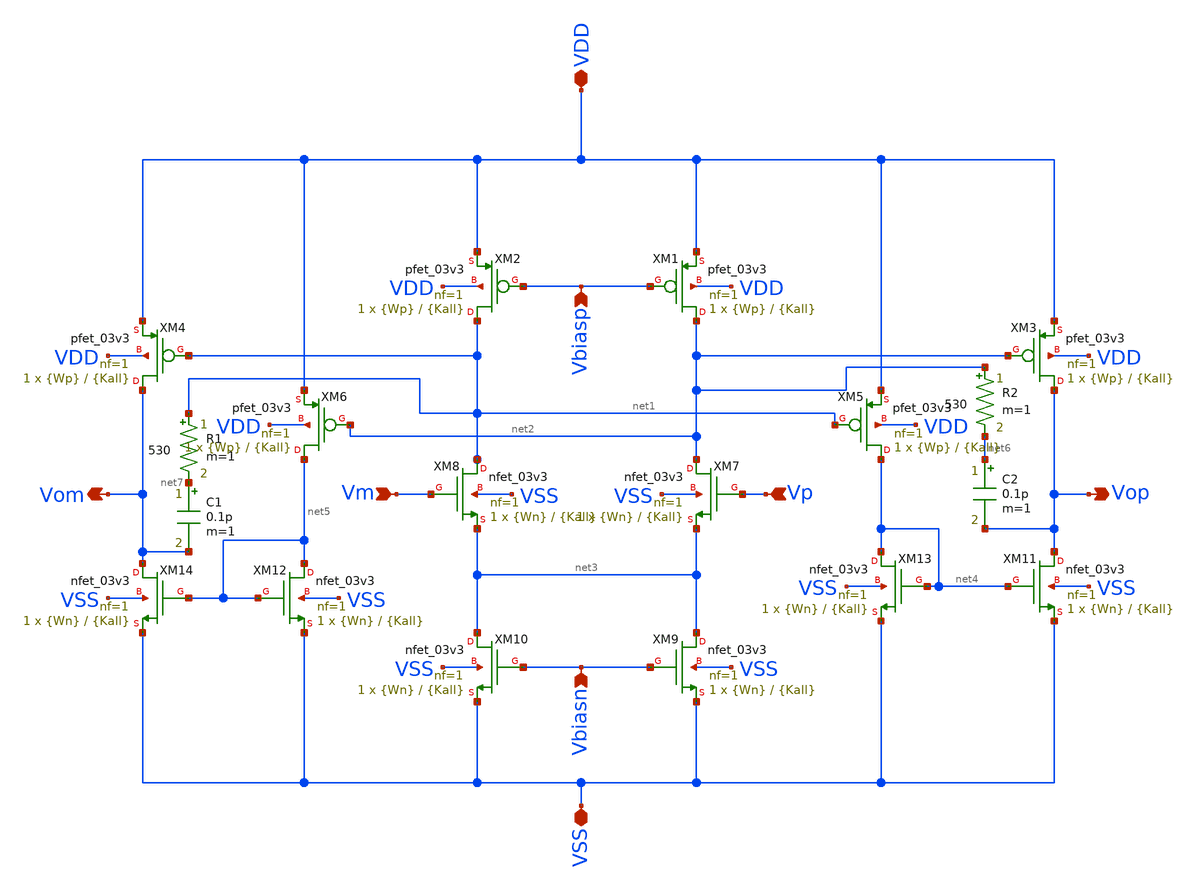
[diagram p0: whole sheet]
** sch_path: src/schematics/fully_differential_amplifier/fullydiffamp.sch
**.subckt fullydiffamp VDD VSS Vbiasn Vbiasp Vm Vp Vom Vop
*.iopin VDD
*.iopin VSS
*.ipin Vbiasn
*.ipin Vbiasp
*.ipin Vm
*.ipin Vp
*.opin Vom
*.opin Vop
XM5 net4 net1 VDD VDD pfet_03v3 L={Kall} W={Wp} nf=1 ad='int((nf+1)/2) * W/nf * 0.18u' as='int((nf+2)/2) * W/nf * 0.18u'
+ pd='2*int((nf+1)/2) * (W/nf + 0.18u)' ps='2*int((nf+2)/2) * (W/nf + 0.18u)' nrd='0.18u / W' nrs='0.18u / W'
+ sa=0 sb=0 sd=0 m=1
XM2 net1 Vbiasp VDD VDD pfet_03v3 L={Kall} W={Wp} nf=1 ad='int((nf+1)/2) * W/nf * 0.18u' as='int((nf+2)/2) * W/nf * 0.18u'
+ pd='2*int((nf+1)/2) * (W/nf + 0.18u)' ps='2*int((nf+2)/2) * (W/nf + 0.18u)' nrd='0.18u / W' nrs='0.18u / W'
+ sa=0 sb=0 sd=0 m=1
XM8 net1 Vm net3 VSS nfet_03v3 L={Kall} W={Wn} nf=1 ad='int((nf+1)/2) * W/nf * 0.18u' as='int((nf+2)/2) * W/nf * 0.18u'
+ pd='2*int((nf+1)/2) * (W/nf + 0.18u)' ps='2*int((nf+2)/2) * (W/nf + 0.18u)' nrd='0.18u / W' nrs='0.18u / W'
+ sa=0 sb=0 sd=0 m=1
XM7 net2 Vp net3 VSS nfet_03v3 L={Kall} W={Wn} nf=1 ad='int((nf+1)/2) * W/nf * 0.18u' as='int((nf+2)/2) * W/nf * 0.18u'
+ pd='2*int((nf+1)/2) * (W/nf + 0.18u)' ps='2*int((nf+2)/2) * (W/nf + 0.18u)' nrd='0.18u / W' nrs='0.18u / W'
+ sa=0 sb=0 sd=0 m=1
XM1 net2 Vbiasp VDD VDD pfet_03v3 L={Kall} W={Wp} nf=1 ad='int((nf+1)/2) * W/nf * 0.18u' as='int((nf+2)/2) * W/nf * 0.18u'
+ pd='2*int((nf+1)/2) * (W/nf + 0.18u)' ps='2*int((nf+2)/2) * (W/nf + 0.18u)' nrd='0.18u / W' nrs='0.18u / W'
+ sa=0 sb=0 sd=0 m=1
XM6 net5 net2 VDD VDD pfet_03v3 L={Kall} W={Wp} nf=1 ad='int((nf+1)/2) * W/nf * 0.18u' as='int((nf+2)/2) * W/nf * 0.18u'
+ pd='2*int((nf+1)/2) * (W/nf + 0.18u)' ps='2*int((nf+2)/2) * (W/nf + 0.18u)' nrd='0.18u / W' nrs='0.18u / W'
+ sa=0 sb=0 sd=0 m=1
XM4 Vom net1 VDD VDD pfet_03v3 L={Kall} W={Wp} nf=1 ad='int((nf+1)/2) * W/nf * 0.18u' as='int((nf+2)/2) * W/nf * 0.18u'
+ pd='2*int((nf+1)/2) * (W/nf + 0.18u)' ps='2*int((nf+2)/2) * (W/nf + 0.18u)' nrd='0.18u / W' nrs='0.18u / W'
+ sa=0 sb=0 sd=0 m=1
XM3 Vop net2 VDD VDD pfet_03v3 L={Kall} W={Wp} nf=1 ad='int((nf+1)/2) * W/nf * 0.18u' as='int((nf+2)/2) * W/nf * 0.18u'
+ pd='2*int((nf+1)/2) * (W/nf + 0.18u)' ps='2*int((nf+2)/2) * (W/nf + 0.18u)' nrd='0.18u / W' nrs='0.18u / W'
+ sa=0 sb=0 sd=0 m=1
XM9 net3 Vbiasn VSS VSS nfet_03v3 L={Kall} W={Wn} nf=1 ad='int((nf+1)/2) * W/nf * 0.18u' as='int((nf+2)/2) * W/nf * 0.18u'
+ pd='2*int((nf+1)/2) * (W/nf + 0.18u)' ps='2*int((nf+2)/2) * (W/nf + 0.18u)' nrd='0.18u / W' nrs='0.18u / W'
+ sa=0 sb=0 sd=0 m=1
XM10 net3 Vbiasn VSS VSS nfet_03v3 L={Kall} W={Wn} nf=1 ad='int((nf+1)/2) * W/nf * 0.18u' as='int((nf+2)/2) * W/nf * 0.18u'
+ pd='2*int((nf+1)/2) * (W/nf + 0.18u)' ps='2*int((nf+2)/2) * (W/nf + 0.18u)' nrd='0.18u / W' nrs='0.18u / W'
+ sa=0 sb=0 sd=0 m=1
XM11 Vop net4 VSS VSS nfet_03v3 L={Kall} W={Wn} nf=1 ad='int((nf+1)/2) * W/nf * 0.18u' as='int((nf+2)/2) * W/nf * 0.18u'
+ pd='2*int((nf+1)/2) * (W/nf + 0.18u)' ps='2*int((nf+2)/2) * (W/nf + 0.18u)' nrd='0.18u / W' nrs='0.18u / W'
+ sa=0 sb=0 sd=0 m=1
XM13 net4 net4 VSS VSS nfet_03v3 L={Kall} W={Wn} nf=1 ad='int((nf+1)/2) * W/nf * 0.18u' as='int((nf+2)/2) * W/nf * 0.18u'
+ pd='2*int((nf+1)/2) * (W/nf + 0.18u)' ps='2*int((nf+2)/2) * (W/nf + 0.18u)' nrd='0.18u / W' nrs='0.18u / W'
+ sa=0 sb=0 sd=0 m=1
XM12 net5 net5 VSS VSS nfet_03v3 L={Kall} W={Wn} nf=1 ad='int((nf+1)/2) * W/nf * 0.18u' as='int((nf+2)/2) * W/nf * 0.18u'
+ pd='2*int((nf+1)/2) * (W/nf + 0.18u)' ps='2*int((nf+2)/2) * (W/nf + 0.18u)' nrd='0.18u / W' nrs='0.18u / W'
+ sa=0 sb=0 sd=0 m=1
XM14 Vom net5 VSS VSS nfet_03v3 L={Kall} W={Wn} nf=1 ad='int((nf+1)/2) * W/nf * 0.18u' as='int((nf+2)/2) * W/nf * 0.18u'
+ pd='2*int((nf+1)/2) * (W/nf + 0.18u)' ps='2*int((nf+2)/2) * (W/nf + 0.18u)' nrd='0.18u / W' nrs='0.18u / W'
+ sa=0 sb=0 sd=0 m=1
R1 net1 net7 530 m=1
R2 net2 net6 530 m=1
C1 net7 Vom 0.1p m=1
C2 net6 Vop 0.1p m=1
**.ends
.end
